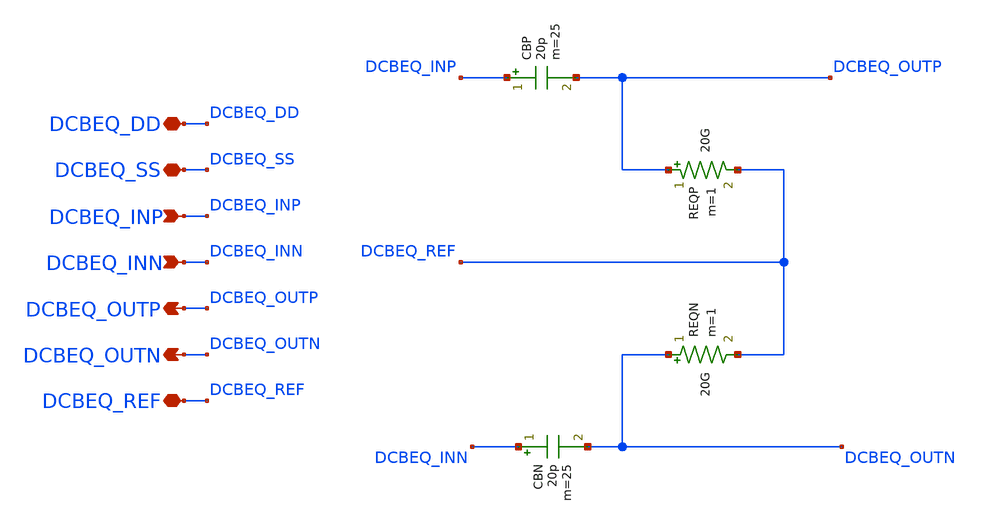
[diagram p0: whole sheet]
** sch_path: Design_Files/IC Design/Schematic/DCB_EQ/DCB_EQ.sch
**.subckt DCB_EQ DCBEQ_DD DCBEQ_SS DCBEQ_INP DCBEQ_INN DCBEQ_OUTP DCBEQ_OUTN DCBEQ_REF
*.iopin DCBEQ_DD
*.iopin DCBEQ_SS
*.ipin DCBEQ_INP
*.ipin DCBEQ_INN
*.opin DCBEQ_OUTP
*.opin DCBEQ_OUTN
*.iopin DCBEQ_REF
CBP DCBEQ_INP DCBEQ_OUTP 20p m=25
CBN DCBEQ_INN DCBEQ_OUTN 20p m=25
REQP DCBEQ_OUTP DCBEQ_REF 20G m=1
REQN DCBEQ_OUTN DCBEQ_REF 20G m=1
**.ends
.end
